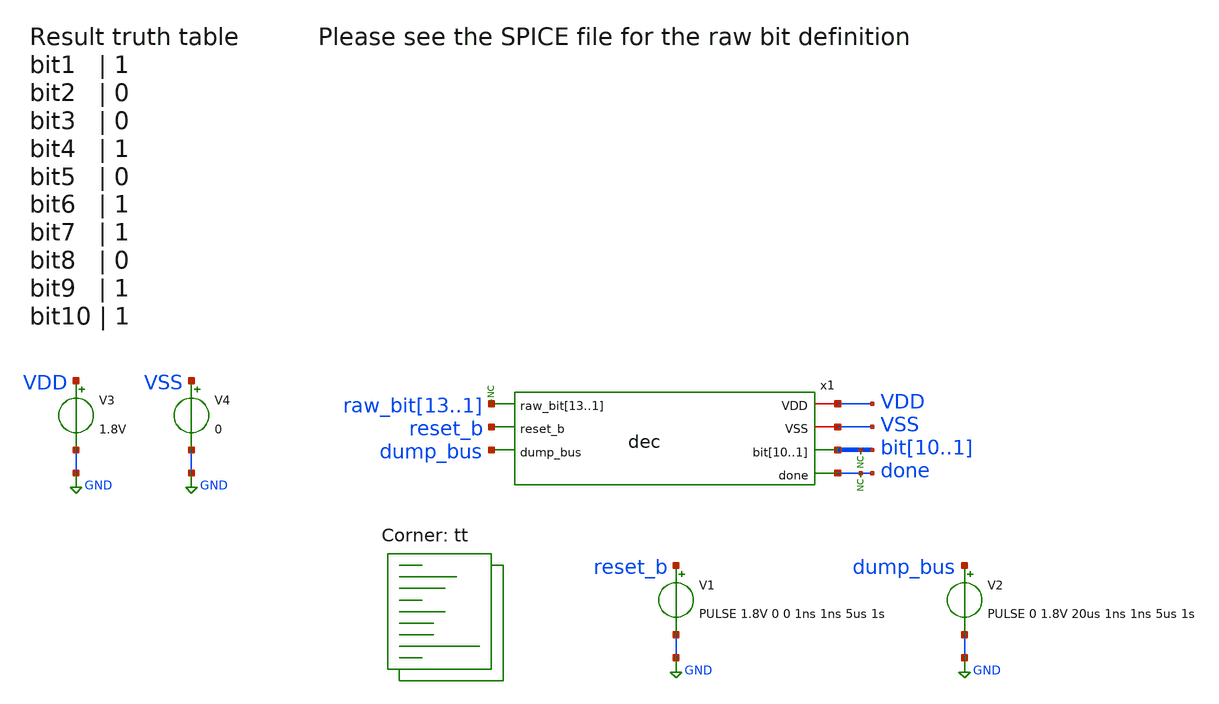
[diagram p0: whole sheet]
** sch_path: xschem/tests/dec/dec_test.sch
**.subckt dec_test
V3 VDD GND 1.8V
V4 VSS GND 0
x1 VDD raw_bit13 raw_bit12 raw_bit11 raw_bit10 raw_bit9 raw_bit8 raw_bit7 raw_bit6 raw_bit5 raw_bit4
+ raw_bit3 raw_bit2 raw_bit1 VSS reset_b bit10 bit9 bit8 bit7 bit6 bit5 bit4 bit3 bit2 bit1 done dump_bus dec
V1 reset_b GND PULSE 1.8V 0 0 1ns 1ns 5us 1s
V2 dump_bus GND PULSE 0 1.8V 20us 1ns 1ns 5us 1s
* noconn done
* noconn bit[10..1]
* noconn raw_bit[13..1]
**** begin user architecture code
 *.lib $::SKYWATER_MODELS/sky130.lib.spice tt
.include $::SKYWATER_STDCELLS/sky130_fd_sc_hd.spice


.options acct list
.temp 25
*vvcc VDD 0 dc 1.8

* * Create the input raw bits
v_ref1 raw_bit1 0 dc 1.8
v_ref2 raw_bit2 0 dc 0
v_ref3 raw_bit3 0 dc 1.8
v_ref4 raw_bit4 0 dc 0
v_ref5 raw_bit5 0 dc 1.8
v_ref6 raw_bit6 0 dc 0
v_ref7 raw_bit7 0 dc 1.8
v_ref8 raw_bit8 0 dc 0
v_ref9 raw_bit9 0 dc 1.8
v_ref10 raw_bit10 0 dc 0
v_ref11 raw_bit11 0 dc 1.8
v_ref12 raw_bit12 0 dc 0
v_ref13 raw_bit13 0 dc 1.8



* Create the input raw bits
* v_ref1 raw_bit1 0 dc 1.8
* v_ref2 raw_bit2 0 dc 1.8
* v_ref3 raw_bit3 0 dc 1.8
* v_ref4 raw_bit4 0 dc 1.8
* v_ref5 raw_bit5 0 dc 1.8
* v_ref6 raw_bit6 0 dc 1.8
* v_ref7 raw_bit7 0 dc 1.8
* v_ref8 raw_bit8 0 dc 1.8
* v_ref9 raw_bit9 0 dc 1.8
* v_ref10 raw_bit10 0 dc 1.8
* v_ref11 raw_bit11 0 dc 1.8
* v_ref12 raw_bit12 0 dc 1.8
* v_ref13 raw_bit13 0 dc 1.8




*vvss VSS 0 0
.control
save all
tran 0.1u 50u
plot reset_b dump_bus+2 done+4 bit10+6 bit9+8 bit8+10
plot bit10 bit9+2 bit8+4 bit7+6 bit6+8 bit5+10 bit4+12 bit3+14 bit2+16 bit1+18
write dec_test.raw
.endc


.lib $::SKYWATER_MODELS/sky130.lib.spice tt
**** end user architecture code
**.ends

* expanding   symbol:  src/dec/dec.sym # of pins=7
** sym_path: xschem/src/dec/dec.sym
** sch_path: xschem/src/dec/dec.sch
.subckt dec VDD raw_bit13 raw_bit12 raw_bit11 raw_bit10 raw_bit9 raw_bit8 raw_bit7 raw_bit6 raw_bit5
+ raw_bit4 raw_bit3 raw_bit2 raw_bit1 VSS reset_b bit10 bit9 bit8 bit7 bit6 bit5 bit4 bit3 bit2 bit1 done
+ dump_bus
*.iopin VDD
*.iopin VSS
*.ipin reset_b
*.ipin dump_bus
*.opin done
*.ipin raw_bit13
*.ipin raw_bit12
*.ipin raw_bit11
*.ipin raw_bit10
*.ipin raw_bit9
*.ipin raw_bit8
*.ipin raw_bit7
*.ipin raw_bit6
*.ipin raw_bit5
*.ipin raw_bit4
*.ipin raw_bit3
*.ipin raw_bit2
*.ipin raw_bit1
*.opin bit10
*.opin bit9
*.opin bit8
*.opin bit7
*.opin bit6
*.opin bit5
*.opin bit4
*.opin bit3
*.opin bit2
*.opin bit1
x62 raw_bit2 raw_bit1 net1 VSS VSS VDD VDD net16 net2 sky130_fd_sc_hd__fa_1
x64 raw_bit3 raw_bit1 net4 VSS VSS VDD VDD net1 net3 sky130_fd_sc_hd__fa_1
x67 dump_bus net2 reset_b VSS VSS VDD VDD bit2 sky130_fd_sc_hd__dfrtp_1
x68 dump_bus net3 reset_b VSS VSS VDD VDD bit3 sky130_fd_sc_hd__dfrtp_1
x65 raw_bit5 raw_bit4 net5 VSS VSS VDD VDD net4 net6 sky130_fd_sc_hd__fa_1
x69 raw_bit6 raw_bit4 net8 VSS VSS VDD VDD net5 net7 sky130_fd_sc_hd__fa_1
x70 dump_bus net6 reset_b VSS VSS VDD VDD bit4 sky130_fd_sc_hd__dfrtp_1
x71 dump_bus net7 reset_b VSS VSS VDD VDD bit5 sky130_fd_sc_hd__dfrtp_1
x72 raw_bit7 raw_bit4 net9 VSS VSS VDD VDD net8 net10 sky130_fd_sc_hd__fa_1
x73 raw_bit9 raw_bit8 net12 VSS VSS VDD VDD net9 net11 sky130_fd_sc_hd__fa_1
x74 dump_bus net10 reset_b VSS VSS VDD VDD bit6 sky130_fd_sc_hd__dfrtp_1
x75 dump_bus net11 reset_b VSS VSS VDD VDD bit7 sky130_fd_sc_hd__dfrtp_1
x76 raw_bit10 raw_bit8 net13 VSS VSS VDD VDD net12 net14 sky130_fd_sc_hd__fa_1
x77 raw_bit11 raw_bit8 raw_bit12 VSS VSS VDD VDD net13 net15 sky130_fd_sc_hd__fa_1
x78 dump_bus net14 reset_b VSS VSS VDD VDD bit8 sky130_fd_sc_hd__dfrtp_1
x79 dump_bus net15 reset_b VSS VSS VDD VDD bit9 sky130_fd_sc_hd__dfrtp_1
x80 dump_bus net16 reset_b VSS VSS VDD VDD bit1 sky130_fd_sc_hd__dfrtp_1
x81 dump_bus raw_bit13 reset_b VSS VSS VDD VDD bit10 sky130_fd_sc_hd__dfrtp_1
x82 dump_bus VSS VSS VDD VDD done sky130_fd_sc_hd__inv_1
* noconn done
.ends

.GLOBAL GND
.end
